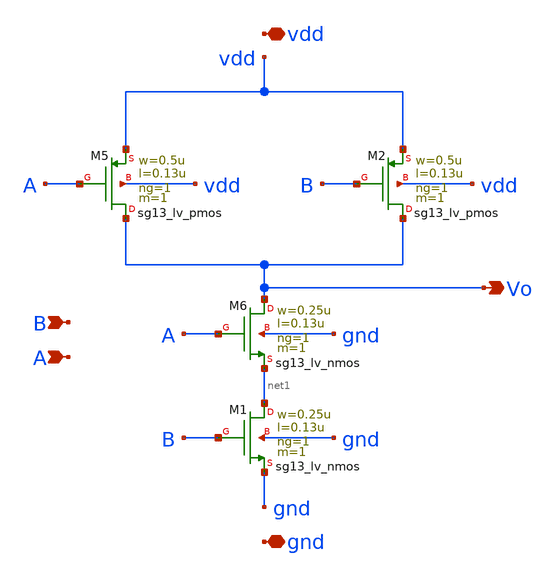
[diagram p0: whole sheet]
** sch_path: modules/module_3_8_bit_SAR_ADC/part_2_digital_comps/nand_gate/schematic/nand_gate.sch
**.subckt nand_gate vdd gnd A Vo B
*.iopin vdd
*.iopin gnd
*.ipin A
*.opin Vo
*.ipin B
XM5 Vo A vdd vdd sg13_lv_pmos w=0.5u l=0.13u ng=1 m=1 mm_ok=1
XM6 Vo A net1 gnd sg13_lv_nmos w=0.25u l=0.13u ng=1 m=1 mm_ok=1
XM1 net1 B gnd gnd sg13_lv_nmos w=0.25u l=0.13u ng=1 m=1 mm_ok=1
XM2 Vo B vdd vdd sg13_lv_pmos w=0.5u l=0.13u ng=1 m=1 mm_ok=1
**.ends
.end
